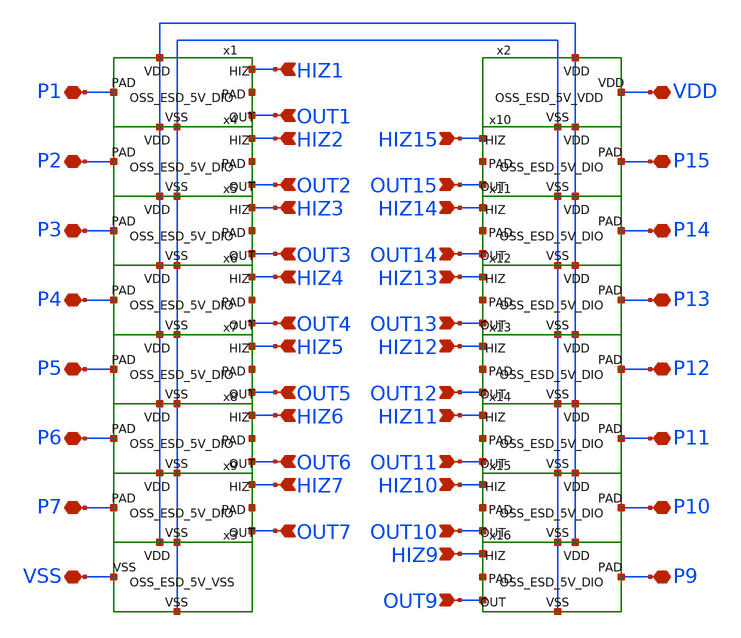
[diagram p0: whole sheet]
** sch_path: libs.tech/xschem/TR-1um_frame/OSS_FRAME_GIO.sch
**.subckt OSS_FRAME_GIO P1 P2 P3 P4 P5 P6 P7 VSS VDD P15 P14 P13 P12 P11 P10 P9 HIZ1 OUT1 HIZ2 OUT2
*+ HIZ3 OUT3 HIZ4 OUT4 HIZ5 OUT5 HIZ6 OUT6 HIZ7 OUT7 HIZ15 OUT15 HIZ14 OUT14 HIZ13 OUT13 HIZ12 OUT12 HIZ11
*+ OUT11 HIZ10 OUT10 HIZ9 OUT9
*.iopin P1
*.iopin P2
*.iopin P3
*.iopin P4
*.iopin P5
*.iopin P6
*.iopin P7
*.iopin VSS
*.iopin VDD
*.iopin P15
*.iopin P14
*.iopin P13
*.iopin P12
*.iopin P11
*.iopin P10
*.iopin P9
*.ipin HIZ1
*.ipin OUT1
*.ipin HIZ2
*.ipin OUT2
*.ipin HIZ3
*.ipin OUT3
*.ipin HIZ4
*.ipin OUT4
*.ipin HIZ5
*.ipin OUT5
*.ipin HIZ6
*.ipin OUT6
*.ipin HIZ7
*.ipin OUT7
*.ipin HIZ15
*.ipin OUT15
*.ipin HIZ14
*.ipin OUT14
*.ipin HIZ13
*.ipin OUT13
*.ipin HIZ12
*.ipin OUT12
*.ipin HIZ11
*.ipin OUT11
*.ipin HIZ10
*.ipin OUT10
*.ipin HIZ9
*.ipin OUT9
x1 VDD P1 VSS HIZ1 OUT1 OSS_ESD_5V_DIO
x2 VDD VSS OSS_ESD_5V_VDD
x3 VDD VSS OSS_ESD_5V_VSS
x4 VDD P2 VSS HIZ2 OUT2 OSS_ESD_5V_DIO
x5 VDD P3 VSS HIZ3 OUT3 OSS_ESD_5V_DIO
x6 VDD P4 VSS HIZ4 OUT4 OSS_ESD_5V_DIO
x7 VDD P5 VSS HIZ5 OUT5 OSS_ESD_5V_DIO
x8 VDD P6 VSS HIZ6 OUT6 OSS_ESD_5V_DIO
x9 VDD P7 VSS HIZ7 OUT7 OSS_ESD_5V_DIO
x10 VDD P15 VSS HIZ15 OUT15 OSS_ESD_5V_DIO
x11 VDD P14 VSS HIZ14 OUT14 OSS_ESD_5V_DIO
x12 VDD P13 VSS HIZ13 OUT13 OSS_ESD_5V_DIO
x13 VDD P12 VSS HIZ12 OUT12 OSS_ESD_5V_DIO
x14 VDD P11 VSS HIZ11 OUT11 OSS_ESD_5V_DIO
x15 VDD P10 VSS HIZ10 OUT10 OSS_ESD_5V_DIO
x16 VDD P9 VSS HIZ9 OUT9 OSS_ESD_5V_DIO
**.ends

* expanding   symbol:  OSS_ESD_5V_DIO.sym # of pins=6
** sym_path: libs.tech/xschem/TR-1um_frame/OSS_ESD_5V_DIO.sym
** sch_path: libs.tech/xschem/TR-1um_frame/OSS_ESD_5V_DIO.sch
.subckt OSS_ESD_5V_DIO VDD PAD VSS HIZ OUT
*.iopin PAD
*.iopin VDD
*.iopin VSS
*.ipin HIZ
*.ipin OUT
XXM1 PAD PG VDD VDD MPE w=300u l=2u as=0 ad=0 ps=0 pd=0 nrd=0 nrs=0 m=1
XXM2 PAD NG VSS VSS MNE w=150u l=2u as=0 ad=0 ps=0 pd=0 nrd=0 nrs=0 m=1
XXM3 PG PGG VDD VDD PMOS w=20.8u l=1u nrd=0 nrs=0 m=1
XXM4 PG PGG VSS VSS NMOS w=6.8u l=1u nrd=0 nrs=0 m=1
XXM5 PAD VDD VDD VDD MPE w=200u l=2u as=0 ad=0 ps=0 pd=0 nrd=0 nrs=0 m=1
XXM6 PAD VSS VSS VSS MNE w=350u l=2u as=0 ad=0 ps=0 pd=0 nrd=0 nrs=0 m=1
XXM7 NG NGG VDD VDD PMOS w=19.4u l=1u nrd=0 nrs=0 m=1
XXM8 NG NGG VSS VSS NMOS w=6.8u l=1u nrd=0 nrs=0 m=1
XXM9 PGG HIZ net2 VDD PMOS w=10.4u l=1u nrd=0 nrs=0 m=1
XXM10 net2 net1 VDD VDD PMOS w=10.4u l=1u nrd=0 nrs=0 m=1
XXM11 PGG net1 VSS VSS NMOS w=3.4u l=1u nrd=0 nrs=0 m=1
XXM12 PGG HIZ VSS VSS NMOS w=3.4u l=1u nrd=0 nrs=0 m=1
XXM13 NGG net1 VDD VDD PMOS w=5.2u l=1u nrd=0 nrs=0 m=1
XXM14 NGG ENB VDD VDD PMOS w=5.2u l=1u nrd=0 nrs=0 m=1
XXM15 NGG ENB net3 VSS NMOS w=3.4u l=1u nrd=0 nrs=0 m=1
XXM16 net3 net1 VSS VSS NMOS w=3.4u l=1u nrd=0 nrs=0 m=1
XXM17 ENB HIZ VDD VDD PMOS w=5.2u l=1u nrd=0 nrs=0 m=1
XXM18 ENB HIZ VSS VSS NMOS w=3.4u l=1u nrd=0 nrs=0 m=1
DD1 VSS HIZ DN m=1
XXM19 net1 OUT VDD VDD PMOS w=5.2u l=1u nrd=0 nrs=0 m=1
XXM20 net1 OUT VSS VSS NMOS w=3.4u l=1u nrd=0 nrs=0 m=1
DD2 VSS OUT DN m=1
.ends


* expanding   symbol:  OSS_ESD_5V_VDD.sym # of pins=3
** sym_path: libs.tech/xschem/TR-1um_frame/OSS_ESD_5V_VDD.sym
** sch_path: libs.tech/xschem/TR-1um_frame/OSS_ESD_5V_VDD.sch
.subckt OSS_ESD_5V_VDD VDD VSS
*.iopin VSS
*.iopin VDD
*.iopin VDD
XXM5 VSS VDD VDD VDD MPE w=500u l=2u as=0 ad=0 ps=0 pd=0 nrd=0 nrs=0 m=1
XXM6 VDD VSS VSS VSS MNE w=500u l=2u as=0 ad=0 ps=0 pd=0 nrd=0 nrs=0 m=1
.ends


* expanding   symbol:  OSS_ESD_5V_VSS.sym # of pins=3
** sym_path: libs.tech/xschem/TR-1um_frame/OSS_ESD_5V_VSS.sym
** sch_path: libs.tech/xschem/TR-1um_frame/OSS_ESD_5V_VSS.sch
.subckt OSS_ESD_5V_VSS VDD VSS
*.iopin VSS
*.iopin VDD
XXM1 VSS VDD VDD VDD MPE w=500u l=2u as=0 ad=0 ps=0 pd=0 nrd=0 nrs=0 m=1
XXM2 VSS VSS VSS VSS MNE w=500u l=2u as=0 ad=0 ps=0 pd=0 nrd=0 nrs=0 m=1
.ends

.end
